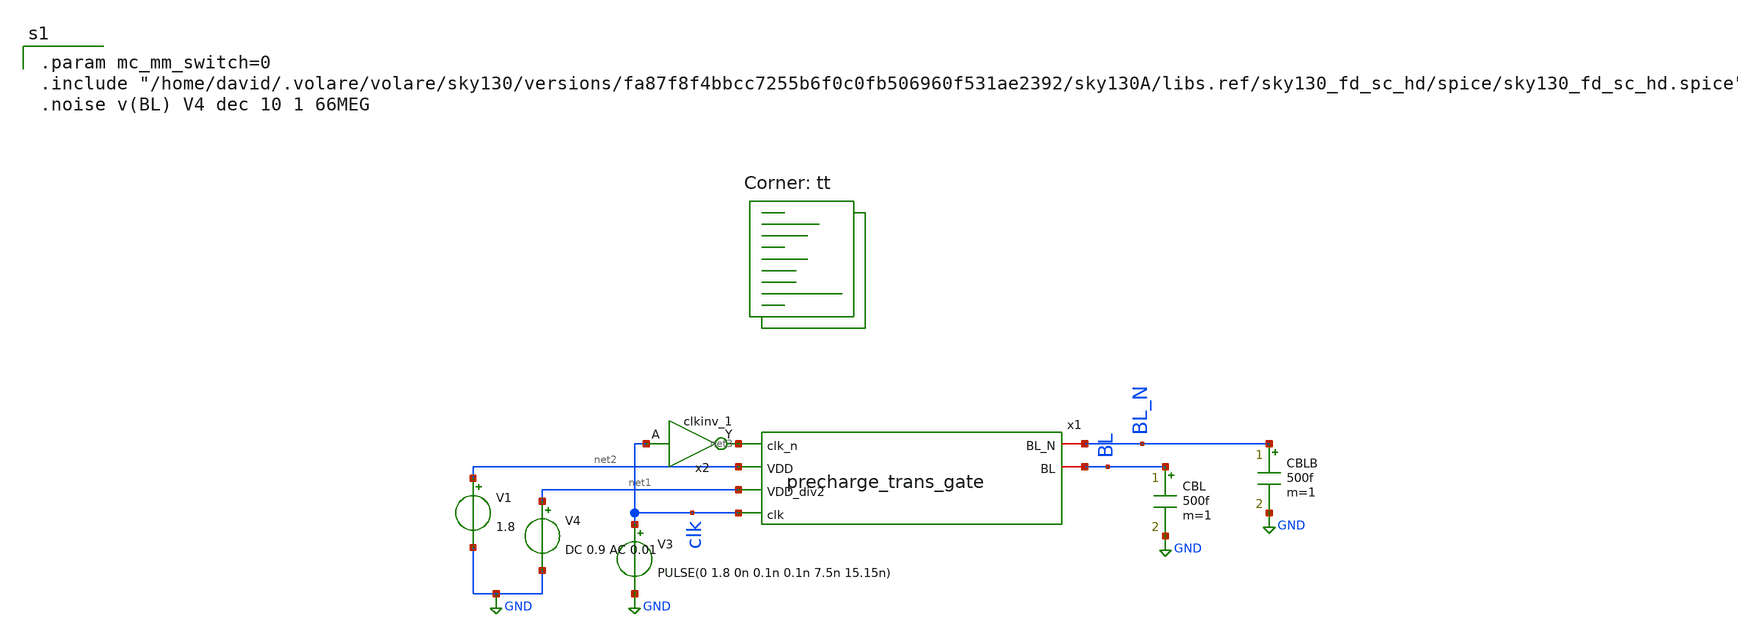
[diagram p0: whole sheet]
** sch_path: analog/schematics/trans_gate_tb.sch
**.subckt trans_gate_tb
V3 clk GND PULSE(0 1.8 0n 0.1n 0.1n 7.5n 15.15n)
x2 clk VGND VNB VPB VPWR net3 sky130_fd_sc_hd__clkinv_1
V4 net1 GND DC 0.9 AC 0.01
CBLB BL_N GND 500f m=1
CBL BL GND 500f m=1
x1 net3 BL_N BL net2 net1 clk precharge_trans_gate
V1 net2 GND 1.8
**** begin user architecture code

.param mc_mm_switch=0
.include "/home/david/.volare/volare/sky130/versions/fa87f8f4bbcc7255b6f0c0fb506960f531ae2392/sky130A/libs.ref/sky130_fd_sc_hd/spice/sky130_fd_sc_hd.spice"
.noise v(BL) V4 dec 10 1 66MEG

.lib $::SKYWATER_MODELS/sky130.lib.spice tt
**** end user architecture code
**.ends
.GLOBAL GND
.end
